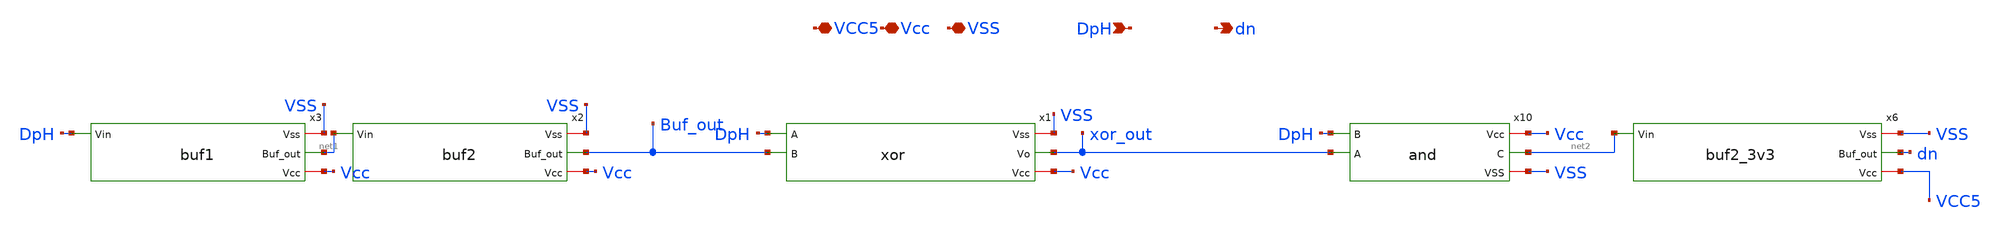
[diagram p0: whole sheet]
** sch_path: Git Files/Schematic/PreEmphasisDriverNetlist_1v8_3v3.sch
**.subckt PreEmphasisDriverNetlist_1v8_3v3 DpH dn VSS Vcc VCC5
*.ipin DpH
*.opin dn
*.iopin VSS
*.iopin Vcc
*.iopin VCC5
x1 VSS DpH xor_out Buf_out Vcc xor
x10 Vcc DpH xor_out net2 VSS and
x2 VSS net1 Buf_out Vcc buf2
x3 VSS DpH net1 Vcc buf1
x6 VSS net2 dn VCC5 buf2_3v3
**.ends
.end
